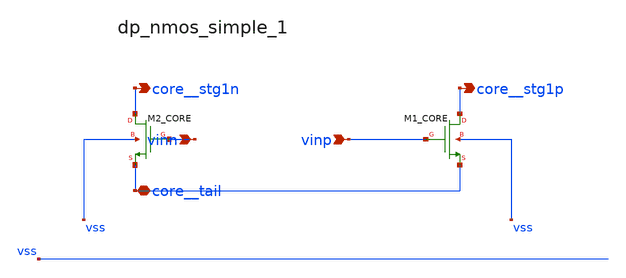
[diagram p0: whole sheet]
** sch_path: analog-db/raw/amp_030_miller_cmfb_composite/hier/blocks/dp_nmos_simple_1.sch
**.subckt dp_nmos_simple_1 vinn vinp core__tail core__stg1n core__stg1p
*.ipin vinn
*.ipin vinp
*.iopin core__tail
*.opin core__stg1n
*.opin core__stg1p
XM1_CORE core__stg1p vinp core__tail vss sg13_lv_nmos w=x_dut_xm1_core_w l=x_dut_xm1_core_l ng=1
+ m=x_dut_xm1_core_m
XM2_CORE core__stg1n vinn core__tail vss sg13_lv_nmos w=x_dut_xm2_core_w l=x_dut_xm2_core_l ng=1
+ m=x_dut_xm2_core_m
**.ends
.end
